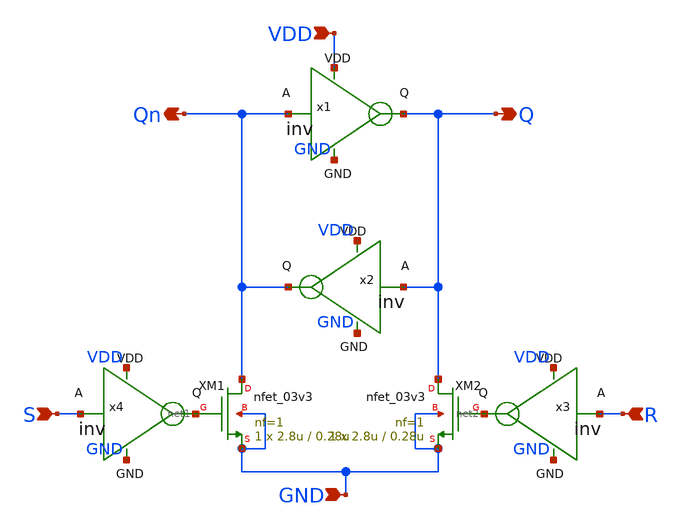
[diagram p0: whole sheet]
** sch_path: latch/latch.sch
**.subckt latch Q Qn GND VDD S R
*.opin Q
*.opin Qn
*.ipin GND
*.ipin VDD
*.ipin S
*.ipin R
x1 VDD Qn Q GND inv
x2 VDD Q Qn GND inv
XM1 Qn net1 GND GND nfet_03v3 L=0.28u W=2.8u nf=1 ad='int((nf+1)/2) * W/nf * 0.18u' as='int((nf+2)/2) * W/nf * 0.18u'
+ pd='2*int((nf+1)/2) * (W/nf + 0.18u)' ps='2*int((nf+2)/2) * (W/nf + 0.18u)' nrd='0.18u / W' nrs='0.18u / W'
+ sa=0 sb=0 sd=0 m=1
XM2 Q net2 GND GND nfet_03v3 L=0.28u W=2.8u nf=1 ad='int((nf+1)/2) * W/nf * 0.18u' as='int((nf+2)/2) * W/nf * 0.18u'
+ pd='2*int((nf+1)/2) * (W/nf + 0.18u)' ps='2*int((nf+2)/2) * (W/nf + 0.18u)' nrd='0.18u / W' nrs='0.18u / W'
+ sa=0 sb=0 sd=0 m=1
x3 VDD R net2 GND inv
x4 VDD S net1 GND inv
**.ends

* expanding   symbol:  inverter/inv.sym # of pins=4
** sym_path: review/0407/inverter/inv.sym
** sch_path: review/0407/inverter/inv.sch
.subckt inv VDD A Q GND
*.ipin A
*.opin Q
*.iopin VDD
*.iopin GND
XM1 Q A VDD VDD pfet_03v3 L=0.28u W=2.8u nf=1 ad='int((nf+1)/2) * W/nf * 0.18u' as='int((nf+2)/2) * W/nf * 0.18u'
+ pd='2*int((nf+1)/2) * (W/nf + 0.18u)' ps='2*int((nf+2)/2) * (W/nf + 0.18u)' nrd='0.18u / W' nrs='0.18u / W'
+ sa=0 sb=0 sd=0 m=1
XM2 Q A GND GND nfet_03v3 L=0.28u W=2.8u nf=1 ad='int((nf+1)/2) * W/nf * 0.18u' as='int((nf+2)/2) * W/nf * 0.18u'
+ pd='2*int((nf+1)/2) * (W/nf + 0.18u)' ps='2*int((nf+2)/2) * (W/nf + 0.18u)' nrd='0.18u / W' nrs='0.18u / W'
+ sa=0 sb=0 sd=0 m=1
.ends

.end
